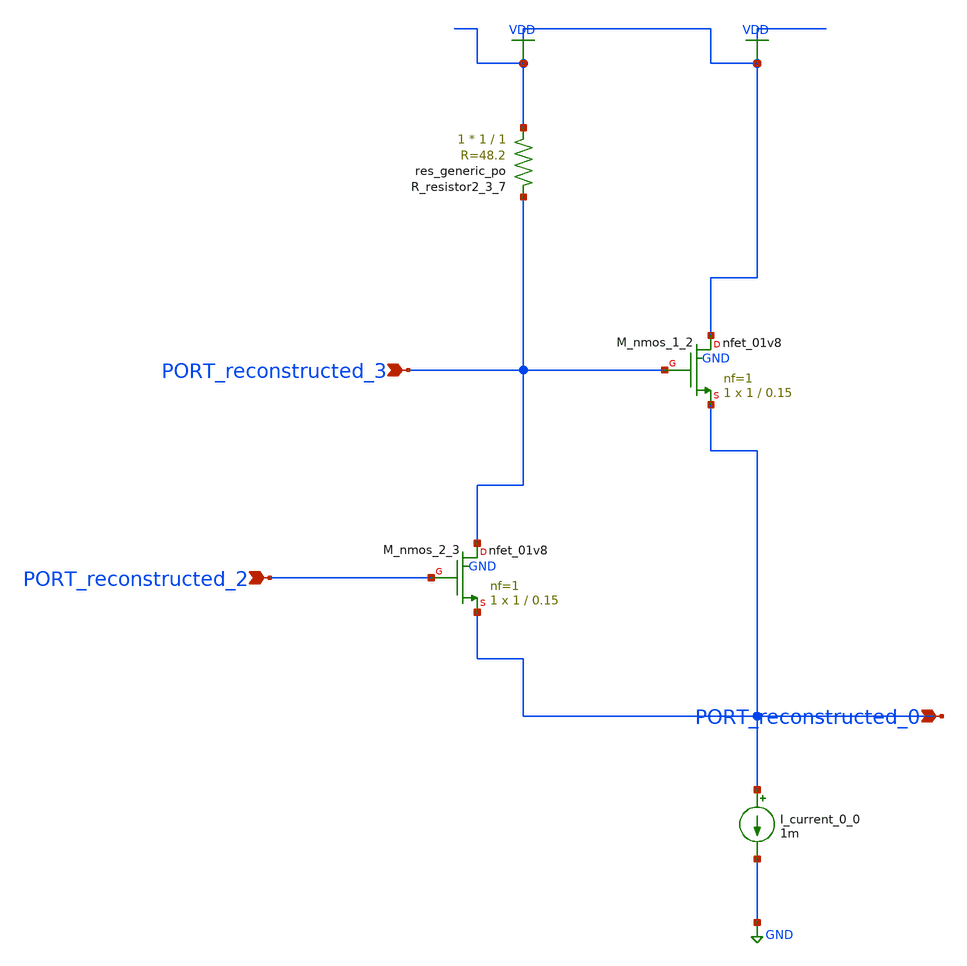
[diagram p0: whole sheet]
** sch_path: schematics/AMSNet/523.sch
**.subckt 523 PORT_reconstructed_0 PORT_reconstructed_2 PORT_reconstructed_3
*.ipin PORT_reconstructed_0
*.ipin PORT_reconstructed_2
*.ipin PORT_reconstructed_3
I_current_0_0 PORT_reconstructed_0 GND 1m
XM_nmos_1_2 VDD PORT_reconstructed_3 PORT_reconstructed_0 GND sky130_fd_pr__nfet_01v8 L=0.15 W=1 nf=1
+ ad='int((1 + 1)/2) * 1 / 1 * 0.29' as='int((1 + 2)/2) * 1 / 1 * 0.29' pd='2*int((1 + 1)/2) * (1 / 1 + 0.29)'
+ ps='2*int((1 + 2)/2) * (1 / 1 + 0.29)' nrd='0.29 / 1 ' nrs='0.29 / 1 ' sa=0 sb=0 sd=0 mult=1 m=1
XM_nmos_2_3 PORT_reconstructed_3 PORT_reconstructed_2 PORT_reconstructed_0 GND sky130_fd_pr__nfet_01v8
+ L=0.15 W=1 nf=1 ad='int((1 + 1)/2) * 1 / 1 * 0.29' as='int((1 + 2)/2) * 1 / 1 * 0.29' pd='2*int((1 + 1)/2) * (1 / 1 + 0.29)'
+ ps='2*int((1 + 2)/2) * (1 / 1 + 0.29)' nrd='0.29 / 1 ' nrs='0.29 / 1 ' sa=0 sb=0 sd=0 mult=1 m=1
XR_resistor2_3_7 VDD PORT_reconstructed_3 sky130_fd_pr__res_generic_po W=1 L=1 m=1
**.ends
.GLOBAL GND
.GLOBAL VDD
.end
